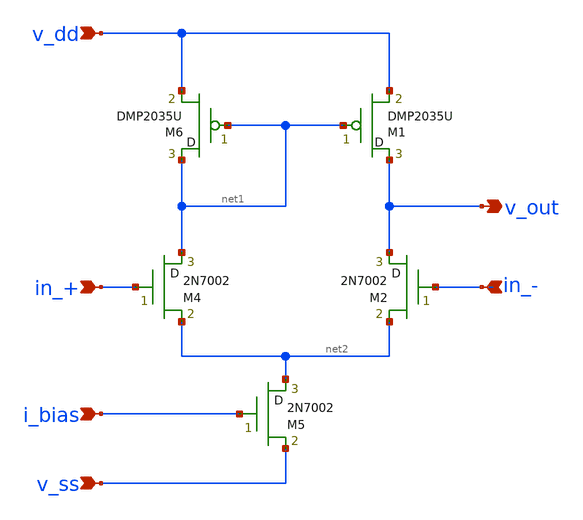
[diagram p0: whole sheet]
** sch_path: 3_Real_Cir/self_build_opamp.sch
**.subckt self_build_opamp in_+ in_- v_ss v_dd i_bias v_out
*.ipin in_+
*.ipin in_-
*.ipin v_ss
*.ipin v_dd
*.ipin i_bias
*.opin v_out
M2 v_out in_- net2 M2N7002 m=1
M4 net1 in_+ net2 M2N7002 m=1
M5 net2 i_bias v_ss M2N7002 m=1
M6 net1 net1 v_dd DMP2035U m=1
M1 v_out net1 v_dd DMP2035U m=1
**.ends
.end
